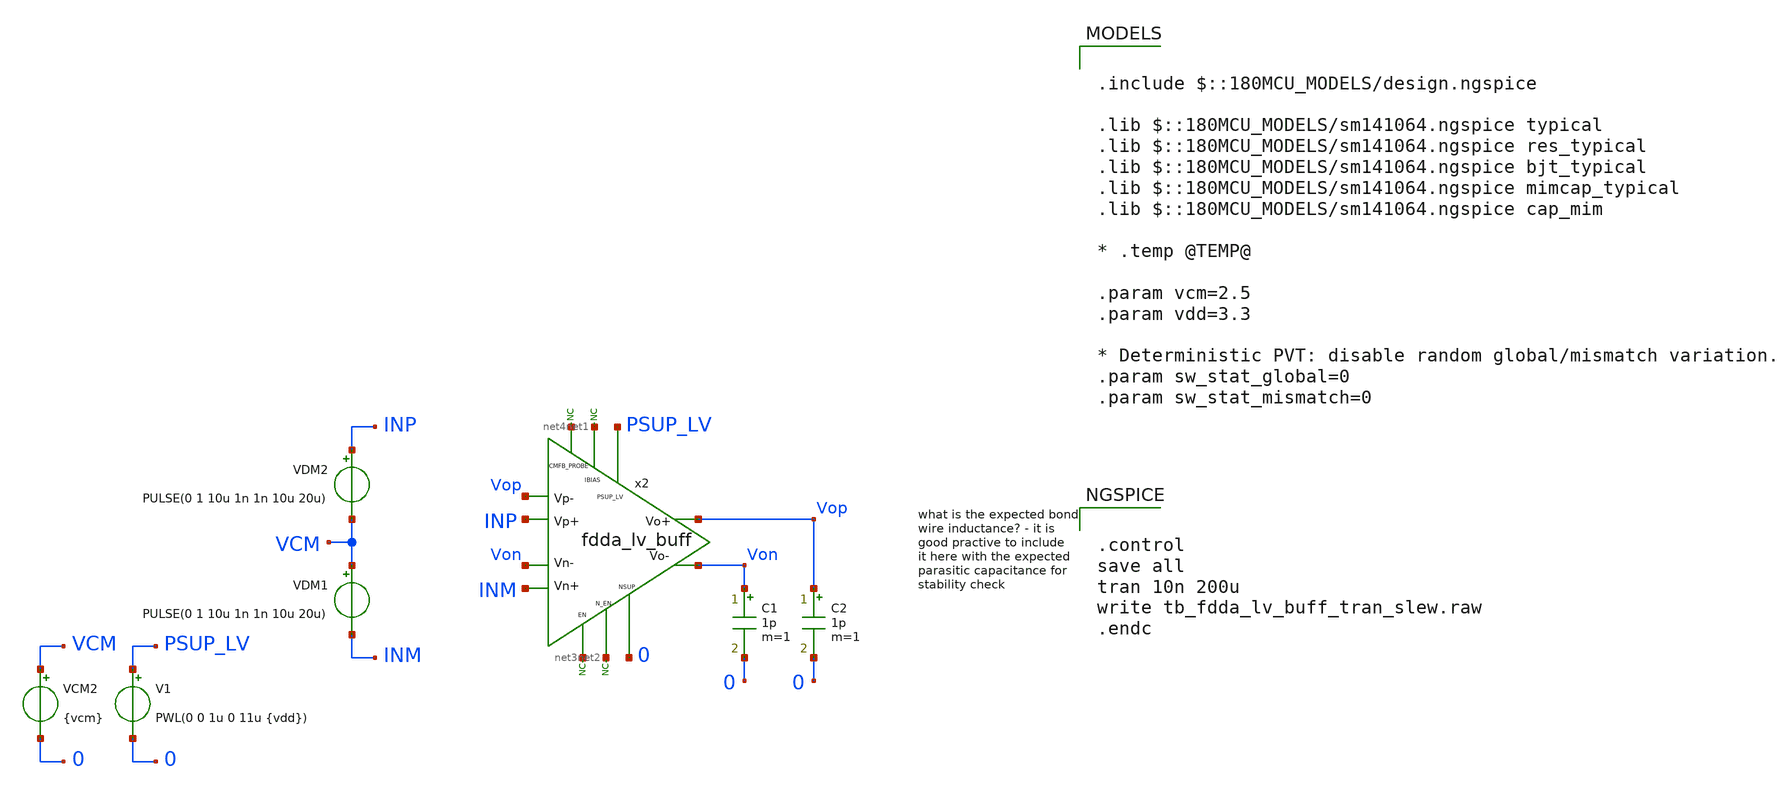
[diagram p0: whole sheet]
** sch_path: xschem/blocks/fdda_lv_buff/tb_fdda_lv_buff_tran_slew.sch
**.subckt tb_fdda_lv_buff_tran_slew
C1 Von 0 1p m=1
x2 PSUP_LV Vop Von INM INP Vop Von net1 net2 net3 0 net4 fdda_lv_buff
* noconn #net1
* noconn #net3
* noconn #net2
V1 PSUP_LV 0 PWL(0 0 1u 0 11u {vdd})
C2 Vop 0 1p m=1
VCM2 VCM 0 {vcm}
VDM2 INP VCM PULSE(0 1 10u 1n 1n 10u 20u)
VDM1 VCM INM PULSE(0 1 10u 1n 1n 10u 20u)
* noconn #net4
**** begin user architecture code

.include $::180MCU_MODELS/design.ngspice

.lib $::180MCU_MODELS/sm141064.ngspice typical
.lib $::180MCU_MODELS/sm141064.ngspice res_typical
.lib $::180MCU_MODELS/sm141064.ngspice bjt_typical
.lib $::180MCU_MODELS/sm141064.ngspice mimcap_typical
.lib $::180MCU_MODELS/sm141064.ngspice cap_mim

* .temp @TEMP@

.param vcm=2.5
.param vdd=3.3

* Deterministic PVT: disable random global/mismatch variation.
.param sw_stat_global=0
.param sw_stat_mismatch=0



.control
save all
tran 10n 200u
write tb_fdda_lv_buff_tran_slew.raw
.endc


**** end user architecture code
**.ends
.end
